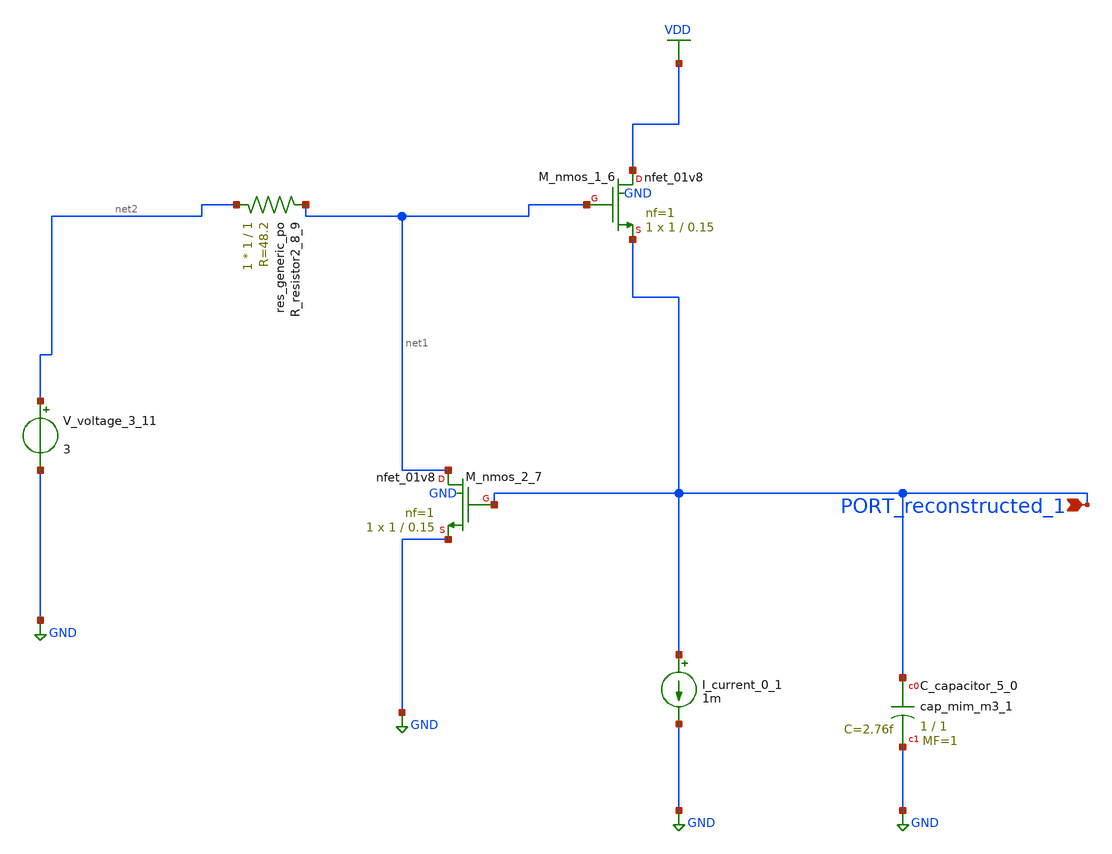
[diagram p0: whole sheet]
** sch_path: schematics/AMSNet/374.sch
**.subckt 374 PORT_reconstructed_1
*.ipin PORT_reconstructed_1
XC_capacitor_5_0 PORT_reconstructed_1 GND sky130_fd_pr__cap_mim_m3_1 W=1 L=1 MF=1 m=1
I_current_0_1 PORT_reconstructed_1 GND 1m
XM_nmos_1_6 VDD net1 PORT_reconstructed_1 GND sky130_fd_pr__nfet_01v8 L=0.15 W=1 nf=1 ad='int((1 + 1)/2) * 1 / 1 * 0.29'
+ as='int((1 + 2)/2) * 1 / 1 * 0.29' pd='2*int((1 + 1)/2) * (1 / 1 + 0.29)' ps='2*int((1 + 2)/2) * (1 / 1 + 0.29)'
+ nrd='0.29 / 1 ' nrs='0.29 / 1 ' sa=0 sb=0 sd=0 mult=1 m=1
XM_nmos_2_7 net1 PORT_reconstructed_1 GND GND sky130_fd_pr__nfet_01v8 L=0.15 W=1 nf=1 ad='int((1 + 1)/2) * 1 / 1 * 0.29'
+ as='int((1 + 2)/2) * 1 / 1 * 0.29' pd='2*int((1 + 1)/2) * (1 / 1 + 0.29)' ps='2*int((1 + 2)/2) * (1 / 1 + 0.29)'
+ nrd='0.29 / 1 ' nrs='0.29 / 1 ' sa=0 sb=0 sd=0 mult=1 m=1
XR_resistor2_8_9 net2 net1 sky130_fd_pr__res_generic_po W=1 L=1 m=1
V_voltage_3_11 net2 GND 3
**.ends
.GLOBAL GND
.GLOBAL VDD
.end
